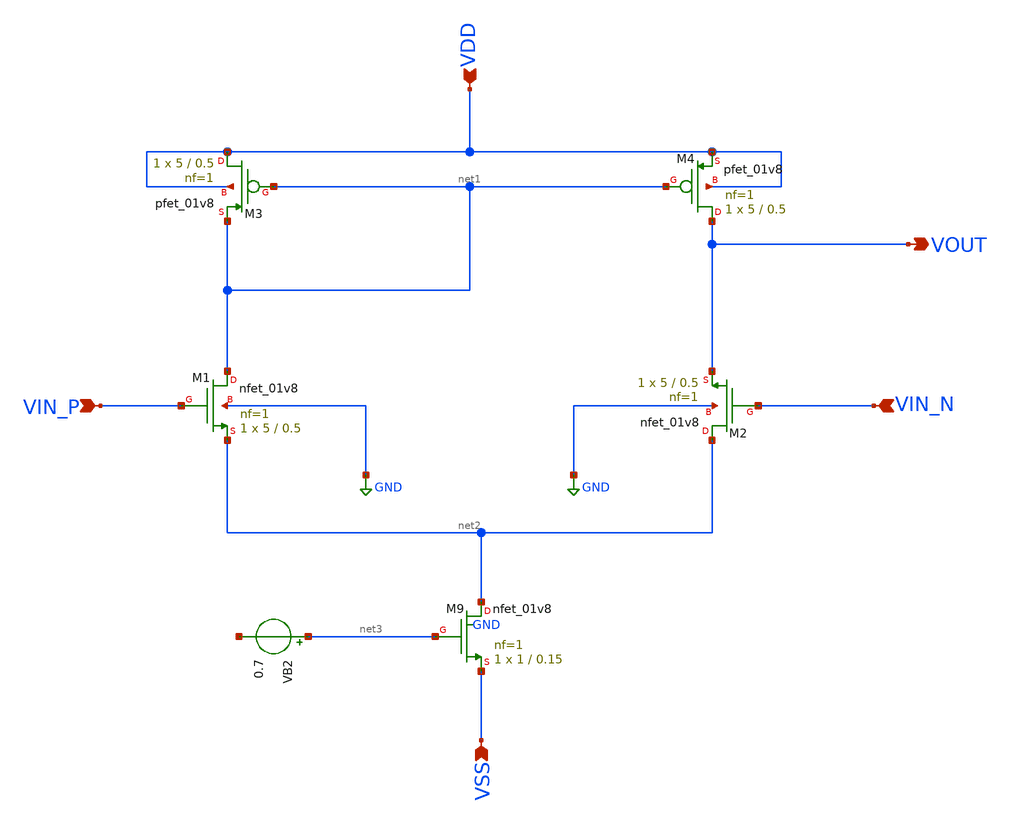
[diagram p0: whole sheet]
** sch_path: analog/schematics/opamp_single_stage.sch
**.subckt opamp_single_stage VIN_P VIN_N VDD VSS VOUT
*.ipin VIN_P
*.ipin VIN_N
*.ipin VDD
*.ipin VSS
*.opin VOUT
XM3 VDD net1 net1 VDD sky130_fd_pr__pfet_01v8 L=0.5 W=5 nf=1 ad='int((nf+1)/2) * W/nf * 0.29' as='int((nf+2)/2) * W/nf * 0.29'
+ pd='2*int((nf+1)/2) * (W/nf + 0.29)' ps='2*int((nf+2)/2) * (W/nf + 0.29)' nrd='0.29 / W' nrs='0.29 / W'
+ sa=0 sb=0 sd=0 mult=1 m=1
XM4 VOUT net1 VDD VDD sky130_fd_pr__pfet_01v8 L=0.5 W=5 nf=1 ad='int((nf+1)/2) * W/nf * 0.29' as='int((nf+2)/2) * W/nf * 0.29'
+ pd='2*int((nf+1)/2) * (W/nf + 0.29)' ps='2*int((nf+2)/2) * (W/nf + 0.29)' nrd='0.29 / W' nrs='0.29 / W'
+ sa=0 sb=0 sd=0 mult=1 m=1
VB2 net3 net4 0.7
XM9 net2 net3 VSS GND sky130_fd_pr__nfet_01v8 L=0.15 W=1 nf=1 ad='int((nf+1)/2) * W/nf * 0.29' as='int((nf+2)/2) * W/nf * 0.29'
+ pd='2*int((nf+1)/2) * (W/nf + 0.29)' ps='2*int((nf+2)/2) * (W/nf + 0.29)' nrd='0.29 / W' nrs='0.29 / W'
+ sa=0 sb=0 sd=0 mult=1 m=1
XM1 net1 VIN_P net2 GND sky130_fd_pr__nfet_01v8 L=0.5 W=5 nf=1 ad='int((nf+1)/2) * W/nf * 0.29' as='int((nf+2)/2) * W/nf * 0.29'
+ pd='2*int((nf+1)/2) * (W/nf + 0.29)' ps='2*int((nf+2)/2) * (W/nf + 0.29)' nrd='0.29 / W' nrs='0.29 / W'
+ sa=0 sb=0 sd=0 mult=1 m=1
XM2 net2 VIN_N VOUT GND sky130_fd_pr__nfet_01v8 L=0.5 W=5 nf=1 ad='int((nf+1)/2) * W/nf * 0.29' as='int((nf+2)/2) * W/nf * 0.29'
+ pd='2*int((nf+1)/2) * (W/nf + 0.29)' ps='2*int((nf+2)/2) * (W/nf + 0.29)' nrd='0.29 / W' nrs='0.29 / W'
+ sa=0 sb=0 sd=0 mult=1 m=1
**.ends
.GLOBAL GND
.end
